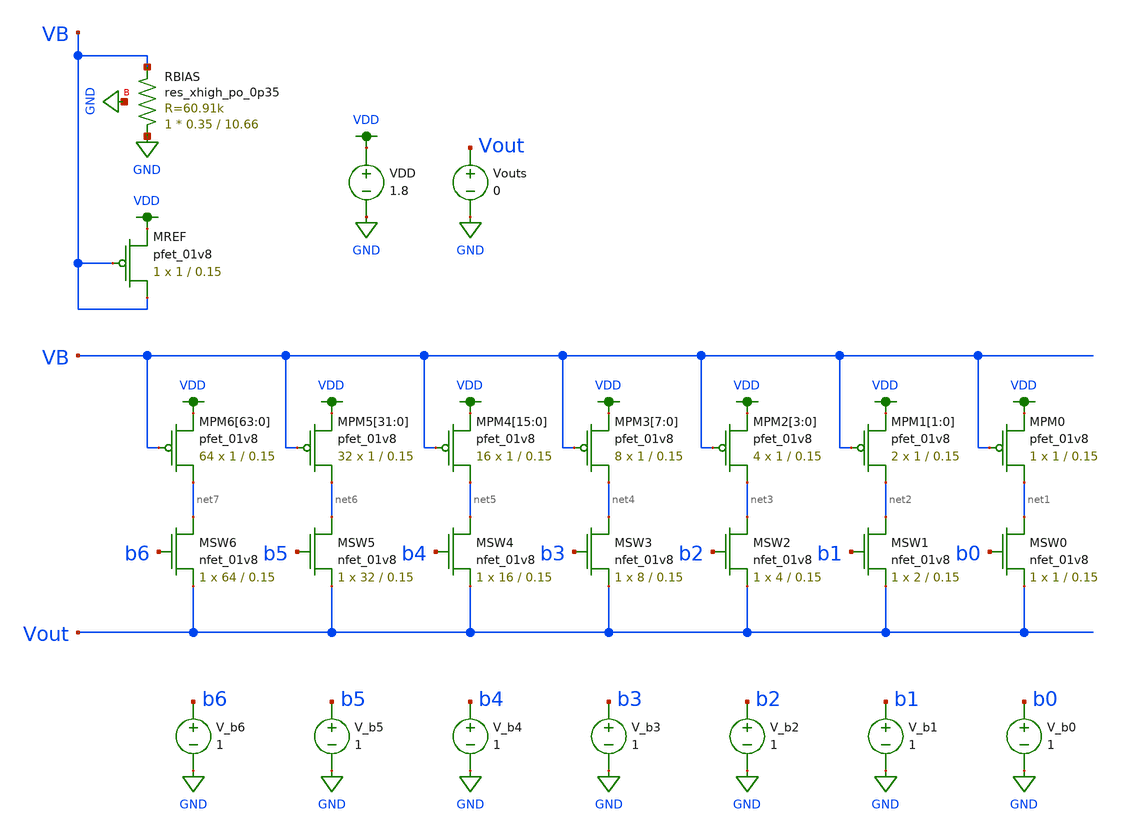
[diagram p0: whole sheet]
** sch_path: MP3/xschem/dac.sch
**.subckt dac
VDD VDD GND 1.8
XMREF VB VB VDD VDD sky130_fd_pr__pfet_01v8 L=0.15 W=1 nf=1 ad='int((nf+1)/2) * W/nf * 0.29' as='int((nf+2)/2) * W/nf * 0.29'
+ pd='2*int((nf+1)/2) * (W/nf + 0.29)' ps='2*int((nf+2)/2) * (W/nf + 0.29)' nrd='0.29 / W' nrs='0.29 / W'
+ sa=0 sb=0 sd=0 mult=1 m=1
XMPM6[63] net7 VB VDD VDD sky130_fd_pr__pfet_01v8 L=0.15 W=1 nf=1 ad='int((nf+1)/2) * W/nf * 0.29' as='int((nf+2)/2) * W/nf * 0.29'
+ pd='2*int((nf+1)/2) * (W/nf + 0.29)' ps='2*int((nf+2)/2) * (W/nf + 0.29)' nrd='0.29 / W' nrs='0.29 / W'
+ sa=0 sb=0 sd=0 mult=64 m=64
XMPM6[62] net7 VB VDD VDD sky130_fd_pr__pfet_01v8 L=0.15 W=1 nf=1 ad='int((nf+1)/2) * W/nf * 0.29' as='int((nf+2)/2) * W/nf * 0.29'
+ pd='2*int((nf+1)/2) * (W/nf + 0.29)' ps='2*int((nf+2)/2) * (W/nf + 0.29)' nrd='0.29 / W' nrs='0.29 / W'
+ sa=0 sb=0 sd=0 mult=64 m=64
XMPM6[61] net7 VB VDD VDD sky130_fd_pr__pfet_01v8 L=0.15 W=1 nf=1 ad='int((nf+1)/2) * W/nf * 0.29' as='int((nf+2)/2) * W/nf * 0.29'
+ pd='2*int((nf+1)/2) * (W/nf + 0.29)' ps='2*int((nf+2)/2) * (W/nf + 0.29)' nrd='0.29 / W' nrs='0.29 / W'
+ sa=0 sb=0 sd=0 mult=64 m=64
XMPM6[60] net7 VB VDD VDD sky130_fd_pr__pfet_01v8 L=0.15 W=1 nf=1 ad='int((nf+1)/2) * W/nf * 0.29' as='int((nf+2)/2) * W/nf * 0.29'
+ pd='2*int((nf+1)/2) * (W/nf + 0.29)' ps='2*int((nf+2)/2) * (W/nf + 0.29)' nrd='0.29 / W' nrs='0.29 / W'
+ sa=0 sb=0 sd=0 mult=64 m=64
XMPM6[59] net7 VB VDD VDD sky130_fd_pr__pfet_01v8 L=0.15 W=1 nf=1 ad='int((nf+1)/2) * W/nf * 0.29' as='int((nf+2)/2) * W/nf * 0.29'
+ pd='2*int((nf+1)/2) * (W/nf + 0.29)' ps='2*int((nf+2)/2) * (W/nf + 0.29)' nrd='0.29 / W' nrs='0.29 / W'
+ sa=0 sb=0 sd=0 mult=64 m=64
XMPM6[58] net7 VB VDD VDD sky130_fd_pr__pfet_01v8 L=0.15 W=1 nf=1 ad='int((nf+1)/2) * W/nf * 0.29' as='int((nf+2)/2) * W/nf * 0.29'
+ pd='2*int((nf+1)/2) * (W/nf + 0.29)' ps='2*int((nf+2)/2) * (W/nf + 0.29)' nrd='0.29 / W' nrs='0.29 / W'
+ sa=0 sb=0 sd=0 mult=64 m=64
XMPM6[57] net7 VB VDD VDD sky130_fd_pr__pfet_01v8 L=0.15 W=1 nf=1 ad='int((nf+1)/2) * W/nf * 0.29' as='int((nf+2)/2) * W/nf * 0.29'
+ pd='2*int((nf+1)/2) * (W/nf + 0.29)' ps='2*int((nf+2)/2) * (W/nf + 0.29)' nrd='0.29 / W' nrs='0.29 / W'
+ sa=0 sb=0 sd=0 mult=64 m=64
XMPM6[56] net7 VB VDD VDD sky130_fd_pr__pfet_01v8 L=0.15 W=1 nf=1 ad='int((nf+1)/2) * W/nf * 0.29' as='int((nf+2)/2) * W/nf * 0.29'
+ pd='2*int((nf+1)/2) * (W/nf + 0.29)' ps='2*int((nf+2)/2) * (W/nf + 0.29)' nrd='0.29 / W' nrs='0.29 / W'
+ sa=0 sb=0 sd=0 mult=64 m=64
XMPM6[55] net7 VB VDD VDD sky130_fd_pr__pfet_01v8 L=0.15 W=1 nf=1 ad='int((nf+1)/2) * W/nf * 0.29' as='int((nf+2)/2) * W/nf * 0.29'
+ pd='2*int((nf+1)/2) * (W/nf + 0.29)' ps='2*int((nf+2)/2) * (W/nf + 0.29)' nrd='0.29 / W' nrs='0.29 / W'
+ sa=0 sb=0 sd=0 mult=64 m=64
XMPM6[54] net7 VB VDD VDD sky130_fd_pr__pfet_01v8 L=0.15 W=1 nf=1 ad='int((nf+1)/2) * W/nf * 0.29' as='int((nf+2)/2) * W/nf * 0.29'
+ pd='2*int((nf+1)/2) * (W/nf + 0.29)' ps='2*int((nf+2)/2) * (W/nf + 0.29)' nrd='0.29 / W' nrs='0.29 / W'
+ sa=0 sb=0 sd=0 mult=64 m=64
XMPM6[53] net7 VB VDD VDD sky130_fd_pr__pfet_01v8 L=0.15 W=1 nf=1 ad='int((nf+1)/2) * W/nf * 0.29' as='int((nf+2)/2) * W/nf * 0.29'
+ pd='2*int((nf+1)/2) * (W/nf + 0.29)' ps='2*int((nf+2)/2) * (W/nf + 0.29)' nrd='0.29 / W' nrs='0.29 / W'
+ sa=0 sb=0 sd=0 mult=64 m=64
XMPM6[52] net7 VB VDD VDD sky130_fd_pr__pfet_01v8 L=0.15 W=1 nf=1 ad='int((nf+1)/2) * W/nf * 0.29' as='int((nf+2)/2) * W/nf * 0.29'
+ pd='2*int((nf+1)/2) * (W/nf + 0.29)' ps='2*int((nf+2)/2) * (W/nf + 0.29)' nrd='0.29 / W' nrs='0.29 / W'
+ sa=0 sb=0 sd=0 mult=64 m=64
XMPM6[51] net7 VB VDD VDD sky130_fd_pr__pfet_01v8 L=0.15 W=1 nf=1 ad='int((nf+1)/2) * W/nf * 0.29' as='int((nf+2)/2) * W/nf * 0.29'
+ pd='2*int((nf+1)/2) * (W/nf + 0.29)' ps='2*int((nf+2)/2) * (W/nf + 0.29)' nrd='0.29 / W' nrs='0.29 / W'
+ sa=0 sb=0 sd=0 mult=64 m=64
XMPM6[50] net7 VB VDD VDD sky130_fd_pr__pfet_01v8 L=0.15 W=1 nf=1 ad='int((nf+1)/2) * W/nf * 0.29' as='int((nf+2)/2) * W/nf * 0.29'
+ pd='2*int((nf+1)/2) * (W/nf + 0.29)' ps='2*int((nf+2)/2) * (W/nf + 0.29)' nrd='0.29 / W' nrs='0.29 / W'
+ sa=0 sb=0 sd=0 mult=64 m=64
XMPM6[49] net7 VB VDD VDD sky130_fd_pr__pfet_01v8 L=0.15 W=1 nf=1 ad='int((nf+1)/2) * W/nf * 0.29' as='int((nf+2)/2) * W/nf * 0.29'
+ pd='2*int((nf+1)/2) * (W/nf + 0.29)' ps='2*int((nf+2)/2) * (W/nf + 0.29)' nrd='0.29 / W' nrs='0.29 / W'
+ sa=0 sb=0 sd=0 mult=64 m=64
XMPM6[48] net7 VB VDD VDD sky130_fd_pr__pfet_01v8 L=0.15 W=1 nf=1 ad='int((nf+1)/2) * W/nf * 0.29' as='int((nf+2)/2) * W/nf * 0.29'
+ pd='2*int((nf+1)/2) * (W/nf + 0.29)' ps='2*int((nf+2)/2) * (W/nf + 0.29)' nrd='0.29 / W' nrs='0.29 / W'
+ sa=0 sb=0 sd=0 mult=64 m=64
XMPM6[47] net7 VB VDD VDD sky130_fd_pr__pfet_01v8 L=0.15 W=1 nf=1 ad='int((nf+1)/2) * W/nf * 0.29' as='int((nf+2)/2) * W/nf * 0.29'
+ pd='2*int((nf+1)/2) * (W/nf + 0.29)' ps='2*int((nf+2)/2) * (W/nf + 0.29)' nrd='0.29 / W' nrs='0.29 / W'
+ sa=0 sb=0 sd=0 mult=64 m=64
XMPM6[46] net7 VB VDD VDD sky130_fd_pr__pfet_01v8 L=0.15 W=1 nf=1 ad='int((nf+1)/2) * W/nf * 0.29' as='int((nf+2)/2) * W/nf * 0.29'
+ pd='2*int((nf+1)/2) * (W/nf + 0.29)' ps='2*int((nf+2)/2) * (W/nf + 0.29)' nrd='0.29 / W' nrs='0.29 / W'
+ sa=0 sb=0 sd=0 mult=64 m=64
XMPM6[45] net7 VB VDD VDD sky130_fd_pr__pfet_01v8 L=0.15 W=1 nf=1 ad='int((nf+1)/2) * W/nf * 0.29' as='int((nf+2)/2) * W/nf * 0.29'
+ pd='2*int((nf+1)/2) * (W/nf + 0.29)' ps='2*int((nf+2)/2) * (W/nf + 0.29)' nrd='0.29 / W' nrs='0.29 / W'
+ sa=0 sb=0 sd=0 mult=64 m=64
XMPM6[44] net7 VB VDD VDD sky130_fd_pr__pfet_01v8 L=0.15 W=1 nf=1 ad='int((nf+1)/2) * W/nf * 0.29' as='int((nf+2)/2) * W/nf * 0.29'
+ pd='2*int((nf+1)/2) * (W/nf + 0.29)' ps='2*int((nf+2)/2) * (W/nf + 0.29)' nrd='0.29 / W' nrs='0.29 / W'
+ sa=0 sb=0 sd=0 mult=64 m=64
XMPM6[43] net7 VB VDD VDD sky130_fd_pr__pfet_01v8 L=0.15 W=1 nf=1 ad='int((nf+1)/2) * W/nf * 0.29' as='int((nf+2)/2) * W/nf * 0.29'
+ pd='2*int((nf+1)/2) * (W/nf + 0.29)' ps='2*int((nf+2)/2) * (W/nf + 0.29)' nrd='0.29 / W' nrs='0.29 / W'
+ sa=0 sb=0 sd=0 mult=64 m=64
XMPM6[42] net7 VB VDD VDD sky130_fd_pr__pfet_01v8 L=0.15 W=1 nf=1 ad='int((nf+1)/2) * W/nf * 0.29' as='int((nf+2)/2) * W/nf * 0.29'
+ pd='2*int((nf+1)/2) * (W/nf + 0.29)' ps='2*int((nf+2)/2) * (W/nf + 0.29)' nrd='0.29 / W' nrs='0.29 / W'
+ sa=0 sb=0 sd=0 mult=64 m=64
XMPM6[41] net7 VB VDD VDD sky130_fd_pr__pfet_01v8 L=0.15 W=1 nf=1 ad='int((nf+1)/2) * W/nf * 0.29' as='int((nf+2)/2) * W/nf * 0.29'
+ pd='2*int((nf+1)/2) * (W/nf + 0.29)' ps='2*int((nf+2)/2) * (W/nf + 0.29)' nrd='0.29 / W' nrs='0.29 / W'
+ sa=0 sb=0 sd=0 mult=64 m=64
XMPM6[40] net7 VB VDD VDD sky130_fd_pr__pfet_01v8 L=0.15 W=1 nf=1 ad='int((nf+1)/2) * W/nf * 0.29' as='int((nf+2)/2) * W/nf * 0.29'
+ pd='2*int((nf+1)/2) * (W/nf + 0.29)' ps='2*int((nf+2)/2) * (W/nf + 0.29)' nrd='0.29 / W' nrs='0.29 / W'
+ sa=0 sb=0 sd=0 mult=64 m=64
XMPM6[39] net7 VB VDD VDD sky130_fd_pr__pfet_01v8 L=0.15 W=1 nf=1 ad='int((nf+1)/2) * W/nf * 0.29' as='int((nf+2)/2) * W/nf * 0.29'
+ pd='2*int((nf+1)/2) * (W/nf + 0.29)' ps='2*int((nf+2)/2) * (W/nf + 0.29)' nrd='0.29 / W' nrs='0.29 / W'
+ sa=0 sb=0 sd=0 mult=64 m=64
XMPM6[38] net7 VB VDD VDD sky130_fd_pr__pfet_01v8 L=0.15 W=1 nf=1 ad='int((nf+1)/2) * W/nf * 0.29' as='int((nf+2)/2) * W/nf * 0.29'
+ pd='2*int((nf+1)/2) * (W/nf + 0.29)' ps='2*int((nf+2)/2) * (W/nf + 0.29)' nrd='0.29 / W' nrs='0.29 / W'
+ sa=0 sb=0 sd=0 mult=64 m=64
XMPM6[37] net7 VB VDD VDD sky130_fd_pr__pfet_01v8 L=0.15 W=1 nf=1 ad='int((nf+1)/2) * W/nf * 0.29' as='int((nf+2)/2) * W/nf * 0.29'
+ pd='2*int((nf+1)/2) * (W/nf + 0.29)' ps='2*int((nf+2)/2) * (W/nf + 0.29)' nrd='0.29 / W' nrs='0.29 / W'
+ sa=0 sb=0 sd=0 mult=64 m=64
XMPM6[36] net7 VB VDD VDD sky130_fd_pr__pfet_01v8 L=0.15 W=1 nf=1 ad='int((nf+1)/2) * W/nf * 0.29' as='int((nf+2)/2) * W/nf * 0.29'
+ pd='2*int((nf+1)/2) * (W/nf + 0.29)' ps='2*int((nf+2)/2) * (W/nf + 0.29)' nrd='0.29 / W' nrs='0.29 / W'
+ sa=0 sb=0 sd=0 mult=64 m=64
XMPM6[35] net7 VB VDD VDD sky130_fd_pr__pfet_01v8 L=0.15 W=1 nf=1 ad='int((nf+1)/2) * W/nf * 0.29' as='int((nf+2)/2) * W/nf * 0.29'
+ pd='2*int((nf+1)/2) * (W/nf + 0.29)' ps='2*int((nf+2)/2) * (W/nf + 0.29)' nrd='0.29 / W' nrs='0.29 / W'
+ sa=0 sb=0 sd=0 mult=64 m=64
XMPM6[34] net7 VB VDD VDD sky130_fd_pr__pfet_01v8 L=0.15 W=1 nf=1 ad='int((nf+1)/2) * W/nf * 0.29' as='int((nf+2)/2) * W/nf * 0.29'
+ pd='2*int((nf+1)/2) * (W/nf + 0.29)' ps='2*int((nf+2)/2) * (W/nf + 0.29)' nrd='0.29 / W' nrs='0.29 / W'
+ sa=0 sb=0 sd=0 mult=64 m=64
XMPM6[33] net7 VB VDD VDD sky130_fd_pr__pfet_01v8 L=0.15 W=1 nf=1 ad='int((nf+1)/2) * W/nf * 0.29' as='int((nf+2)/2) * W/nf * 0.29'
+ pd='2*int((nf+1)/2) * (W/nf + 0.29)' ps='2*int((nf+2)/2) * (W/nf + 0.29)' nrd='0.29 / W' nrs='0.29 / W'
+ sa=0 sb=0 sd=0 mult=64 m=64
XMPM6[32] net7 VB VDD VDD sky130_fd_pr__pfet_01v8 L=0.15 W=1 nf=1 ad='int((nf+1)/2) * W/nf * 0.29' as='int((nf+2)/2) * W/nf * 0.29'
+ pd='2*int((nf+1)/2) * (W/nf + 0.29)' ps='2*int((nf+2)/2) * (W/nf + 0.29)' nrd='0.29 / W' nrs='0.29 / W'
+ sa=0 sb=0 sd=0 mult=64 m=64
XMPM6[31] net7 VB VDD VDD sky130_fd_pr__pfet_01v8 L=0.15 W=1 nf=1 ad='int((nf+1)/2) * W/nf * 0.29' as='int((nf+2)/2) * W/nf * 0.29'
+ pd='2*int((nf+1)/2) * (W/nf + 0.29)' ps='2*int((nf+2)/2) * (W/nf + 0.29)' nrd='0.29 / W' nrs='0.29 / W'
+ sa=0 sb=0 sd=0 mult=64 m=64
XMPM6[30] net7 VB VDD VDD sky130_fd_pr__pfet_01v8 L=0.15 W=1 nf=1 ad='int((nf+1)/2) * W/nf * 0.29' as='int((nf+2)/2) * W/nf * 0.29'
+ pd='2*int((nf+1)/2) * (W/nf + 0.29)' ps='2*int((nf+2)/2) * (W/nf + 0.29)' nrd='0.29 / W' nrs='0.29 / W'
+ sa=0 sb=0 sd=0 mult=64 m=64
XMPM6[29] net7 VB VDD VDD sky130_fd_pr__pfet_01v8 L=0.15 W=1 nf=1 ad='int((nf+1)/2) * W/nf * 0.29' as='int((nf+2)/2) * W/nf * 0.29'
+ pd='2*int((nf+1)/2) * (W/nf + 0.29)' ps='2*int((nf+2)/2) * (W/nf + 0.29)' nrd='0.29 / W' nrs='0.29 / W'
+ sa=0 sb=0 sd=0 mult=64 m=64
XMPM6[28] net7 VB VDD VDD sky130_fd_pr__pfet_01v8 L=0.15 W=1 nf=1 ad='int((nf+1)/2) * W/nf * 0.29' as='int((nf+2)/2) * W/nf * 0.29'
+ pd='2*int((nf+1)/2) * (W/nf + 0.29)' ps='2*int((nf+2)/2) * (W/nf + 0.29)' nrd='0.29 / W' nrs='0.29 / W'
+ sa=0 sb=0 sd=0 mult=64 m=64
XMPM6[27] net7 VB VDD VDD sky130_fd_pr__pfet_01v8 L=0.15 W=1 nf=1 ad='int((nf+1)/2) * W/nf * 0.29' as='int((nf+2)/2) * W/nf * 0.29'
+ pd='2*int((nf+1)/2) * (W/nf + 0.29)' ps='2*int((nf+2)/2) * (W/nf + 0.29)' nrd='0.29 / W' nrs='0.29 / W'
+ sa=0 sb=0 sd=0 mult=64 m=64
XMPM6[26] net7 VB VDD VDD sky130_fd_pr__pfet_01v8 L=0.15 W=1 nf=1 ad='int((nf+1)/2) * W/nf * 0.29' as='int((nf+2)/2) * W/nf * 0.29'
+ pd='2*int((nf+1)/2) * (W/nf + 0.29)' ps='2*int((nf+2)/2) * (W/nf + 0.29)' nrd='0.29 / W' nrs='0.29 / W'
+ sa=0 sb=0 sd=0 mult=64 m=64
XMPM6[25] net7 VB VDD VDD sky130_fd_pr__pfet_01v8 L=0.15 W=1 nf=1 ad='int((nf+1)/2) * W/nf * 0.29' as='int((nf+2)/2) * W/nf * 0.29'
+ pd='2*int((nf+1)/2) * (W/nf + 0.29)' ps='2*int((nf+2)/2) * (W/nf + 0.29)' nrd='0.29 / W' nrs='0.29 / W'
+ sa=0 sb=0 sd=0 mult=64 m=64
XMPM6[24] net7 VB VDD VDD sky130_fd_pr__pfet_01v8 L=0.15 W=1 nf=1 ad='int((nf+1)/2) * W/nf * 0.29' as='int((nf+2)/2) * W/nf * 0.29'
+ pd='2*int((nf+1)/2) * (W/nf + 0.29)' ps='2*int((nf+2)/2) * (W/nf + 0.29)' nrd='0.29 / W' nrs='0.29 / W'
+ sa=0 sb=0 sd=0 mult=64 m=64
XMPM6[23] net7 VB VDD VDD sky130_fd_pr__pfet_01v8 L=0.15 W=1 nf=1 ad='int((nf+1)/2) * W/nf * 0.29' as='int((nf+2)/2) * W/nf * 0.29'
+ pd='2*int((nf+1)/2) * (W/nf + 0.29)' ps='2*int((nf+2)/2) * (W/nf + 0.29)' nrd='0.29 / W' nrs='0.29 / W'
+ sa=0 sb=0 sd=0 mult=64 m=64
XMPM6[22] net7 VB VDD VDD sky130_fd_pr__pfet_01v8 L=0.15 W=1 nf=1 ad='int((nf+1)/2) * W/nf * 0.29' as='int((nf+2)/2) * W/nf * 0.29'
+ pd='2*int((nf+1)/2) * (W/nf + 0.29)' ps='2*int((nf+2)/2) * (W/nf + 0.29)' nrd='0.29 / W' nrs='0.29 / W'
+ sa=0 sb=0 sd=0 mult=64 m=64
XMPM6[21] net7 VB VDD VDD sky130_fd_pr__pfet_01v8 L=0.15 W=1 nf=1 ad='int((nf+1)/2) * W/nf * 0.29' as='int((nf+2)/2) * W/nf * 0.29'
+ pd='2*int((nf+1)/2) * (W/nf + 0.29)' ps='2*int((nf+2)/2) * (W/nf + 0.29)' nrd='0.29 / W' nrs='0.29 / W'
+ sa=0 sb=0 sd=0 mult=64 m=64
XMPM6[20] net7 VB VDD VDD sky130_fd_pr__pfet_01v8 L=0.15 W=1 nf=1 ad='int((nf+1)/2) * W/nf * 0.29' as='int((nf+2)/2) * W/nf * 0.29'
+ pd='2*int((nf+1)/2) * (W/nf + 0.29)' ps='2*int((nf+2)/2) * (W/nf + 0.29)' nrd='0.29 / W' nrs='0.29 / W'
+ sa=0 sb=0 sd=0 mult=64 m=64
XMPM6[19] net7 VB VDD VDD sky130_fd_pr__pfet_01v8 L=0.15 W=1 nf=1 ad='int((nf+1)/2) * W/nf * 0.29' as='int((nf+2)/2) * W/nf * 0.29'
+ pd='2*int((nf+1)/2) * (W/nf + 0.29)' ps='2*int((nf+2)/2) * (W/nf + 0.29)' nrd='0.29 / W' nrs='0.29 / W'
+ sa=0 sb=0 sd=0 mult=64 m=64
XMPM6[18] net7 VB VDD VDD sky130_fd_pr__pfet_01v8 L=0.15 W=1 nf=1 ad='int((nf+1)/2) * W/nf * 0.29' as='int((nf+2)/2) * W/nf * 0.29'
+ pd='2*int((nf+1)/2) * (W/nf + 0.29)' ps='2*int((nf+2)/2) * (W/nf + 0.29)' nrd='0.29 / W' nrs='0.29 / W'
+ sa=0 sb=0 sd=0 mult=64 m=64
XMPM6[17] net7 VB VDD VDD sky130_fd_pr__pfet_01v8 L=0.15 W=1 nf=1 ad='int((nf+1)/2) * W/nf * 0.29' as='int((nf+2)/2) * W/nf * 0.29'
+ pd='2*int((nf+1)/2) * (W/nf + 0.29)' ps='2*int((nf+2)/2) * (W/nf + 0.29)' nrd='0.29 / W' nrs='0.29 / W'
+ sa=0 sb=0 sd=0 mult=64 m=64
XMPM6[16] net7 VB VDD VDD sky130_fd_pr__pfet_01v8 L=0.15 W=1 nf=1 ad='int((nf+1)/2) * W/nf * 0.29' as='int((nf+2)/2) * W/nf * 0.29'
+ pd='2*int((nf+1)/2) * (W/nf + 0.29)' ps='2*int((nf+2)/2) * (W/nf + 0.29)' nrd='0.29 / W' nrs='0.29 / W'
+ sa=0 sb=0 sd=0 mult=64 m=64
XMPM6[15] net7 VB VDD VDD sky130_fd_pr__pfet_01v8 L=0.15 W=1 nf=1 ad='int((nf+1)/2) * W/nf * 0.29' as='int((nf+2)/2) * W/nf * 0.29'
+ pd='2*int((nf+1)/2) * (W/nf + 0.29)' ps='2*int((nf+2)/2) * (W/nf + 0.29)' nrd='0.29 / W' nrs='0.29 / W'
+ sa=0 sb=0 sd=0 mult=64 m=64
XMPM6[14] net7 VB VDD VDD sky130_fd_pr__pfet_01v8 L=0.15 W=1 nf=1 ad='int((nf+1)/2) * W/nf * 0.29' as='int((nf+2)/2) * W/nf * 0.29'
+ pd='2*int((nf+1)/2) * (W/nf + 0.29)' ps='2*int((nf+2)/2) * (W/nf + 0.29)' nrd='0.29 / W' nrs='0.29 / W'
+ sa=0 sb=0 sd=0 mult=64 m=64
XMPM6[13] net7 VB VDD VDD sky130_fd_pr__pfet_01v8 L=0.15 W=1 nf=1 ad='int((nf+1)/2) * W/nf * 0.29' as='int((nf+2)/2) * W/nf * 0.29'
+ pd='2*int((nf+1)/2) * (W/nf + 0.29)' ps='2*int((nf+2)/2) * (W/nf + 0.29)' nrd='0.29 / W' nrs='0.29 / W'
+ sa=0 sb=0 sd=0 mult=64 m=64
XMPM6[12] net7 VB VDD VDD sky130_fd_pr__pfet_01v8 L=0.15 W=1 nf=1 ad='int((nf+1)/2) * W/nf * 0.29' as='int((nf+2)/2) * W/nf * 0.29'
+ pd='2*int((nf+1)/2) * (W/nf + 0.29)' ps='2*int((nf+2)/2) * (W/nf + 0.29)' nrd='0.29 / W' nrs='0.29 / W'
+ sa=0 sb=0 sd=0 mult=64 m=64
XMPM6[11] net7 VB VDD VDD sky130_fd_pr__pfet_01v8 L=0.15 W=1 nf=1 ad='int((nf+1)/2) * W/nf * 0.29' as='int((nf+2)/2) * W/nf * 0.29'
+ pd='2*int((nf+1)/2) * (W/nf + 0.29)' ps='2*int((nf+2)/2) * (W/nf + 0.29)' nrd='0.29 / W' nrs='0.29 / W'
+ sa=0 sb=0 sd=0 mult=64 m=64
XMPM6[10] net7 VB VDD VDD sky130_fd_pr__pfet_01v8 L=0.15 W=1 nf=1 ad='int((nf+1)/2) * W/nf * 0.29' as='int((nf+2)/2) * W/nf * 0.29'
+ pd='2*int((nf+1)/2) * (W/nf + 0.29)' ps='2*int((nf+2)/2) * (W/nf + 0.29)' nrd='0.29 / W' nrs='0.29 / W'
+ sa=0 sb=0 sd=0 mult=64 m=64
XMPM6[9] net7 VB VDD VDD sky130_fd_pr__pfet_01v8 L=0.15 W=1 nf=1 ad='int((nf+1)/2) * W/nf * 0.29' as='int((nf+2)/2) * W/nf * 0.29'
+ pd='2*int((nf+1)/2) * (W/nf + 0.29)' ps='2*int((nf+2)/2) * (W/nf + 0.29)' nrd='0.29 / W' nrs='0.29 / W'
+ sa=0 sb=0 sd=0 mult=64 m=64
XMPM6[8] net7 VB VDD VDD sky130_fd_pr__pfet_01v8 L=0.15 W=1 nf=1 ad='int((nf+1)/2) * W/nf * 0.29' as='int((nf+2)/2) * W/nf * 0.29'
+ pd='2*int((nf+1)/2) * (W/nf + 0.29)' ps='2*int((nf+2)/2) * (W/nf + 0.29)' nrd='0.29 / W' nrs='0.29 / W'
+ sa=0 sb=0 sd=0 mult=64 m=64
XMPM6[7] net7 VB VDD VDD sky130_fd_pr__pfet_01v8 L=0.15 W=1 nf=1 ad='int((nf+1)/2) * W/nf * 0.29' as='int((nf+2)/2) * W/nf * 0.29'
+ pd='2*int((nf+1)/2) * (W/nf + 0.29)' ps='2*int((nf+2)/2) * (W/nf + 0.29)' nrd='0.29 / W' nrs='0.29 / W'
+ sa=0 sb=0 sd=0 mult=64 m=64
XMPM6[6] net7 VB VDD VDD sky130_fd_pr__pfet_01v8 L=0.15 W=1 nf=1 ad='int((nf+1)/2) * W/nf * 0.29' as='int((nf+2)/2) * W/nf * 0.29'
+ pd='2*int((nf+1)/2) * (W/nf + 0.29)' ps='2*int((nf+2)/2) * (W/nf + 0.29)' nrd='0.29 / W' nrs='0.29 / W'
+ sa=0 sb=0 sd=0 mult=64 m=64
XMPM6[5] net7 VB VDD VDD sky130_fd_pr__pfet_01v8 L=0.15 W=1 nf=1 ad='int((nf+1)/2) * W/nf * 0.29' as='int((nf+2)/2) * W/nf * 0.29'
+ pd='2*int((nf+1)/2) * (W/nf + 0.29)' ps='2*int((nf+2)/2) * (W/nf + 0.29)' nrd='0.29 / W' nrs='0.29 / W'
+ sa=0 sb=0 sd=0 mult=64 m=64
XMPM6[4] net7 VB VDD VDD sky130_fd_pr__pfet_01v8 L=0.15 W=1 nf=1 ad='int((nf+1)/2) * W/nf * 0.29' as='int((nf+2)/2) * W/nf * 0.29'
+ pd='2*int((nf+1)/2) * (W/nf + 0.29)' ps='2*int((nf+2)/2) * (W/nf + 0.29)' nrd='0.29 / W' nrs='0.29 / W'
+ sa=0 sb=0 sd=0 mult=64 m=64
XMPM6[3] net7 VB VDD VDD sky130_fd_pr__pfet_01v8 L=0.15 W=1 nf=1 ad='int((nf+1)/2) * W/nf * 0.29' as='int((nf+2)/2) * W/nf * 0.29'
+ pd='2*int((nf+1)/2) * (W/nf + 0.29)' ps='2*int((nf+2)/2) * (W/nf + 0.29)' nrd='0.29 / W' nrs='0.29 / W'
+ sa=0 sb=0 sd=0 mult=64 m=64
XMPM6[2] net7 VB VDD VDD sky130_fd_pr__pfet_01v8 L=0.15 W=1 nf=1 ad='int((nf+1)/2) * W/nf * 0.29' as='int((nf+2)/2) * W/nf * 0.29'
+ pd='2*int((nf+1)/2) * (W/nf + 0.29)' ps='2*int((nf+2)/2) * (W/nf + 0.29)' nrd='0.29 / W' nrs='0.29 / W'
+ sa=0 sb=0 sd=0 mult=64 m=64
XMPM6[1] net7 VB VDD VDD sky130_fd_pr__pfet_01v8 L=0.15 W=1 nf=1 ad='int((nf+1)/2) * W/nf * 0.29' as='int((nf+2)/2) * W/nf * 0.29'
+ pd='2*int((nf+1)/2) * (W/nf + 0.29)' ps='2*int((nf+2)/2) * (W/nf + 0.29)' nrd='0.29 / W' nrs='0.29 / W'
+ sa=0 sb=0 sd=0 mult=64 m=64
XMPM6[0] net7 VB VDD VDD sky130_fd_pr__pfet_01v8 L=0.15 W=1 nf=1 ad='int((nf+1)/2) * W/nf * 0.29' as='int((nf+2)/2) * W/nf * 0.29'
+ pd='2*int((nf+1)/2) * (W/nf + 0.29)' ps='2*int((nf+2)/2) * (W/nf + 0.29)' nrd='0.29 / W' nrs='0.29 / W'
+ sa=0 sb=0 sd=0 mult=64 m=64
XMPM5[31] net6 VB VDD VDD sky130_fd_pr__pfet_01v8 L=0.15 W=1 nf=1 ad='int((nf+1)/2) * W/nf * 0.29' as='int((nf+2)/2) * W/nf * 0.29'
+ pd='2*int((nf+1)/2) * (W/nf + 0.29)' ps='2*int((nf+2)/2) * (W/nf + 0.29)' nrd='0.29 / W' nrs='0.29 / W'
+ sa=0 sb=0 sd=0 mult=32 m=32
XMPM5[30] net6 VB VDD VDD sky130_fd_pr__pfet_01v8 L=0.15 W=1 nf=1 ad='int((nf+1)/2) * W/nf * 0.29' as='int((nf+2)/2) * W/nf * 0.29'
+ pd='2*int((nf+1)/2) * (W/nf + 0.29)' ps='2*int((nf+2)/2) * (W/nf + 0.29)' nrd='0.29 / W' nrs='0.29 / W'
+ sa=0 sb=0 sd=0 mult=32 m=32
XMPM5[29] net6 VB VDD VDD sky130_fd_pr__pfet_01v8 L=0.15 W=1 nf=1 ad='int((nf+1)/2) * W/nf * 0.29' as='int((nf+2)/2) * W/nf * 0.29'
+ pd='2*int((nf+1)/2) * (W/nf + 0.29)' ps='2*int((nf+2)/2) * (W/nf + 0.29)' nrd='0.29 / W' nrs='0.29 / W'
+ sa=0 sb=0 sd=0 mult=32 m=32
XMPM5[28] net6 VB VDD VDD sky130_fd_pr__pfet_01v8 L=0.15 W=1 nf=1 ad='int((nf+1)/2) * W/nf * 0.29' as='int((nf+2)/2) * W/nf * 0.29'
+ pd='2*int((nf+1)/2) * (W/nf + 0.29)' ps='2*int((nf+2)/2) * (W/nf + 0.29)' nrd='0.29 / W' nrs='0.29 / W'
+ sa=0 sb=0 sd=0 mult=32 m=32
XMPM5[27] net6 VB VDD VDD sky130_fd_pr__pfet_01v8 L=0.15 W=1 nf=1 ad='int((nf+1)/2) * W/nf * 0.29' as='int((nf+2)/2) * W/nf * 0.29'
+ pd='2*int((nf+1)/2) * (W/nf + 0.29)' ps='2*int((nf+2)/2) * (W/nf + 0.29)' nrd='0.29 / W' nrs='0.29 / W'
+ sa=0 sb=0 sd=0 mult=32 m=32
XMPM5[26] net6 VB VDD VDD sky130_fd_pr__pfet_01v8 L=0.15 W=1 nf=1 ad='int((nf+1)/2) * W/nf * 0.29' as='int((nf+2)/2) * W/nf * 0.29'
+ pd='2*int((nf+1)/2) * (W/nf + 0.29)' ps='2*int((nf+2)/2) * (W/nf + 0.29)' nrd='0.29 / W' nrs='0.29 / W'
+ sa=0 sb=0 sd=0 mult=32 m=32
XMPM5[25] net6 VB VDD VDD sky130_fd_pr__pfet_01v8 L=0.15 W=1 nf=1 ad='int((nf+1)/2) * W/nf * 0.29' as='int((nf+2)/2) * W/nf * 0.29'
+ pd='2*int((nf+1)/2) * (W/nf + 0.29)' ps='2*int((nf+2)/2) * (W/nf + 0.29)' nrd='0.29 / W' nrs='0.29 / W'
+ sa=0 sb=0 sd=0 mult=32 m=32
XMPM5[24] net6 VB VDD VDD sky130_fd_pr__pfet_01v8 L=0.15 W=1 nf=1 ad='int((nf+1)/2) * W/nf * 0.29' as='int((nf+2)/2) * W/nf * 0.29'
+ pd='2*int((nf+1)/2) * (W/nf + 0.29)' ps='2*int((nf+2)/2) * (W/nf + 0.29)' nrd='0.29 / W' nrs='0.29 / W'
+ sa=0 sb=0 sd=0 mult=32 m=32
XMPM5[23] net6 VB VDD VDD sky130_fd_pr__pfet_01v8 L=0.15 W=1 nf=1 ad='int((nf+1)/2) * W/nf * 0.29' as='int((nf+2)/2) * W/nf * 0.29'
+ pd='2*int((nf+1)/2) * (W/nf + 0.29)' ps='2*int((nf+2)/2) * (W/nf + 0.29)' nrd='0.29 / W' nrs='0.29 / W'
+ sa=0 sb=0 sd=0 mult=32 m=32
XMPM5[22] net6 VB VDD VDD sky130_fd_pr__pfet_01v8 L=0.15 W=1 nf=1 ad='int((nf+1)/2) * W/nf * 0.29' as='int((nf+2)/2) * W/nf * 0.29'
+ pd='2*int((nf+1)/2) * (W/nf + 0.29)' ps='2*int((nf+2)/2) * (W/nf + 0.29)' nrd='0.29 / W' nrs='0.29 / W'
+ sa=0 sb=0 sd=0 mult=32 m=32
XMPM5[21] net6 VB VDD VDD sky130_fd_pr__pfet_01v8 L=0.15 W=1 nf=1 ad='int((nf+1)/2) * W/nf * 0.29' as='int((nf+2)/2) * W/nf * 0.29'
+ pd='2*int((nf+1)/2) * (W/nf + 0.29)' ps='2*int((nf+2)/2) * (W/nf + 0.29)' nrd='0.29 / W' nrs='0.29 / W'
+ sa=0 sb=0 sd=0 mult=32 m=32
XMPM5[20] net6 VB VDD VDD sky130_fd_pr__pfet_01v8 L=0.15 W=1 nf=1 ad='int((nf+1)/2) * W/nf * 0.29' as='int((nf+2)/2) * W/nf * 0.29'
+ pd='2*int((nf+1)/2) * (W/nf + 0.29)' ps='2*int((nf+2)/2) * (W/nf + 0.29)' nrd='0.29 / W' nrs='0.29 / W'
+ sa=0 sb=0 sd=0 mult=32 m=32
XMPM5[19] net6 VB VDD VDD sky130_fd_pr__pfet_01v8 L=0.15 W=1 nf=1 ad='int((nf+1)/2) * W/nf * 0.29' as='int((nf+2)/2) * W/nf * 0.29'
+ pd='2*int((nf+1)/2) * (W/nf + 0.29)' ps='2*int((nf+2)/2) * (W/nf + 0.29)' nrd='0.29 / W' nrs='0.29 / W'
+ sa=0 sb=0 sd=0 mult=32 m=32
XMPM5[18] net6 VB VDD VDD sky130_fd_pr__pfet_01v8 L=0.15 W=1 nf=1 ad='int((nf+1)/2) * W/nf * 0.29' as='int((nf+2)/2) * W/nf * 0.29'
+ pd='2*int((nf+1)/2) * (W/nf + 0.29)' ps='2*int((nf+2)/2) * (W/nf + 0.29)' nrd='0.29 / W' nrs='0.29 / W'
+ sa=0 sb=0 sd=0 mult=32 m=32
XMPM5[17] net6 VB VDD VDD sky130_fd_pr__pfet_01v8 L=0.15 W=1 nf=1 ad='int((nf+1)/2) * W/nf * 0.29' as='int((nf+2)/2) * W/nf * 0.29'
+ pd='2*int((nf+1)/2) * (W/nf + 0.29)' ps='2*int((nf+2)/2) * (W/nf + 0.29)' nrd='0.29 / W' nrs='0.29 / W'
+ sa=0 sb=0 sd=0 mult=32 m=32
XMPM5[16] net6 VB VDD VDD sky130_fd_pr__pfet_01v8 L=0.15 W=1 nf=1 ad='int((nf+1)/2) * W/nf * 0.29' as='int((nf+2)/2) * W/nf * 0.29'
+ pd='2*int((nf+1)/2) * (W/nf + 0.29)' ps='2*int((nf+2)/2) * (W/nf + 0.29)' nrd='0.29 / W' nrs='0.29 / W'
+ sa=0 sb=0 sd=0 mult=32 m=32
XMPM5[15] net6 VB VDD VDD sky130_fd_pr__pfet_01v8 L=0.15 W=1 nf=1 ad='int((nf+1)/2) * W/nf * 0.29' as='int((nf+2)/2) * W/nf * 0.29'
+ pd='2*int((nf+1)/2) * (W/nf + 0.29)' ps='2*int((nf+2)/2) * (W/nf + 0.29)' nrd='0.29 / W' nrs='0.29 / W'
+ sa=0 sb=0 sd=0 mult=32 m=32
XMPM5[14] net6 VB VDD VDD sky130_fd_pr__pfet_01v8 L=0.15 W=1 nf=1 ad='int((nf+1)/2) * W/nf * 0.29' as='int((nf+2)/2) * W/nf * 0.29'
+ pd='2*int((nf+1)/2) * (W/nf + 0.29)' ps='2*int((nf+2)/2) * (W/nf + 0.29)' nrd='0.29 / W' nrs='0.29 / W'
+ sa=0 sb=0 sd=0 mult=32 m=32
XMPM5[13] net6 VB VDD VDD sky130_fd_pr__pfet_01v8 L=0.15 W=1 nf=1 ad='int((nf+1)/2) * W/nf * 0.29' as='int((nf+2)/2) * W/nf * 0.29'
+ pd='2*int((nf+1)/2) * (W/nf + 0.29)' ps='2*int((nf+2)/2) * (W/nf + 0.29)' nrd='0.29 / W' nrs='0.29 / W'
+ sa=0 sb=0 sd=0 mult=32 m=32
XMPM5[12] net6 VB VDD VDD sky130_fd_pr__pfet_01v8 L=0.15 W=1 nf=1 ad='int((nf+1)/2) * W/nf * 0.29' as='int((nf+2)/2) * W/nf * 0.29'
+ pd='2*int((nf+1)/2) * (W/nf + 0.29)' ps='2*int((nf+2)/2) * (W/nf + 0.29)' nrd='0.29 / W' nrs='0.29 / W'
+ sa=0 sb=0 sd=0 mult=32 m=32
XMPM5[11] net6 VB VDD VDD sky130_fd_pr__pfet_01v8 L=0.15 W=1 nf=1 ad='int((nf+1)/2) * W/nf * 0.29' as='int((nf+2)/2) * W/nf * 0.29'
+ pd='2*int((nf+1)/2) * (W/nf + 0.29)' ps='2*int((nf+2)/2) * (W/nf + 0.29)' nrd='0.29 / W' nrs='0.29 / W'
+ sa=0 sb=0 sd=0 mult=32 m=32
XMPM5[10] net6 VB VDD VDD sky130_fd_pr__pfet_01v8 L=0.15 W=1 nf=1 ad='int((nf+1)/2) * W/nf * 0.29' as='int((nf+2)/2) * W/nf * 0.29'
+ pd='2*int((nf+1)/2) * (W/nf + 0.29)' ps='2*int((nf+2)/2) * (W/nf + 0.29)' nrd='0.29 / W' nrs='0.29 / W'
+ sa=0 sb=0 sd=0 mult=32 m=32
XMPM5[9] net6 VB VDD VDD sky130_fd_pr__pfet_01v8 L=0.15 W=1 nf=1 ad='int((nf+1)/2) * W/nf * 0.29' as='int((nf+2)/2) * W/nf * 0.29'
+ pd='2*int((nf+1)/2) * (W/nf + 0.29)' ps='2*int((nf+2)/2) * (W/nf + 0.29)' nrd='0.29 / W' nrs='0.29 / W'
+ sa=0 sb=0 sd=0 mult=32 m=32
XMPM5[8] net6 VB VDD VDD sky130_fd_pr__pfet_01v8 L=0.15 W=1 nf=1 ad='int((nf+1)/2) * W/nf * 0.29' as='int((nf+2)/2) * W/nf * 0.29'
+ pd='2*int((nf+1)/2) * (W/nf + 0.29)' ps='2*int((nf+2)/2) * (W/nf + 0.29)' nrd='0.29 / W' nrs='0.29 / W'
+ sa=0 sb=0 sd=0 mult=32 m=32
XMPM5[7] net6 VB VDD VDD sky130_fd_pr__pfet_01v8 L=0.15 W=1 nf=1 ad='int((nf+1)/2) * W/nf * 0.29' as='int((nf+2)/2) * W/nf * 0.29'
+ pd='2*int((nf+1)/2) * (W/nf + 0.29)' ps='2*int((nf+2)/2) * (W/nf + 0.29)' nrd='0.29 / W' nrs='0.29 / W'
+ sa=0 sb=0 sd=0 mult=32 m=32
XMPM5[6] net6 VB VDD VDD sky130_fd_pr__pfet_01v8 L=0.15 W=1 nf=1 ad='int((nf+1)/2) * W/nf * 0.29' as='int((nf+2)/2) * W/nf * 0.29'
+ pd='2*int((nf+1)/2) * (W/nf + 0.29)' ps='2*int((nf+2)/2) * (W/nf + 0.29)' nrd='0.29 / W' nrs='0.29 / W'
+ sa=0 sb=0 sd=0 mult=32 m=32
XMPM5[5] net6 VB VDD VDD sky130_fd_pr__pfet_01v8 L=0.15 W=1 nf=1 ad='int((nf+1)/2) * W/nf * 0.29' as='int((nf+2)/2) * W/nf * 0.29'
+ pd='2*int((nf+1)/2) * (W/nf + 0.29)' ps='2*int((nf+2)/2) * (W/nf + 0.29)' nrd='0.29 / W' nrs='0.29 / W'
+ sa=0 sb=0 sd=0 mult=32 m=32
XMPM5[4] net6 VB VDD VDD sky130_fd_pr__pfet_01v8 L=0.15 W=1 nf=1 ad='int((nf+1)/2) * W/nf * 0.29' as='int((nf+2)/2) * W/nf * 0.29'
+ pd='2*int((nf+1)/2) * (W/nf + 0.29)' ps='2*int((nf+2)/2) * (W/nf + 0.29)' nrd='0.29 / W' nrs='0.29 / W'
+ sa=0 sb=0 sd=0 mult=32 m=32
XMPM5[3] net6 VB VDD VDD sky130_fd_pr__pfet_01v8 L=0.15 W=1 nf=1 ad='int((nf+1)/2) * W/nf * 0.29' as='int((nf+2)/2) * W/nf * 0.29'
+ pd='2*int((nf+1)/2) * (W/nf + 0.29)' ps='2*int((nf+2)/2) * (W/nf + 0.29)' nrd='0.29 / W' nrs='0.29 / W'
+ sa=0 sb=0 sd=0 mult=32 m=32
XMPM5[2] net6 VB VDD VDD sky130_fd_pr__pfet_01v8 L=0.15 W=1 nf=1 ad='int((nf+1)/2) * W/nf * 0.29' as='int((nf+2)/2) * W/nf * 0.29'
+ pd='2*int((nf+1)/2) * (W/nf + 0.29)' ps='2*int((nf+2)/2) * (W/nf + 0.29)' nrd='0.29 / W' nrs='0.29 / W'
+ sa=0 sb=0 sd=0 mult=32 m=32
XMPM5[1] net6 VB VDD VDD sky130_fd_pr__pfet_01v8 L=0.15 W=1 nf=1 ad='int((nf+1)/2) * W/nf * 0.29' as='int((nf+2)/2) * W/nf * 0.29'
+ pd='2*int((nf+1)/2) * (W/nf + 0.29)' ps='2*int((nf+2)/2) * (W/nf + 0.29)' nrd='0.29 / W' nrs='0.29 / W'
+ sa=0 sb=0 sd=0 mult=32 m=32
XMPM5[0] net6 VB VDD VDD sky130_fd_pr__pfet_01v8 L=0.15 W=1 nf=1 ad='int((nf+1)/2) * W/nf * 0.29' as='int((nf+2)/2) * W/nf * 0.29'
+ pd='2*int((nf+1)/2) * (W/nf + 0.29)' ps='2*int((nf+2)/2) * (W/nf + 0.29)' nrd='0.29 / W' nrs='0.29 / W'
+ sa=0 sb=0 sd=0 mult=32 m=32
XMPM4[15] net5 VB VDD VDD sky130_fd_pr__pfet_01v8 L=0.15 W=1 nf=1 ad='int((nf+1)/2) * W/nf * 0.29' as='int((nf+2)/2) * W/nf * 0.29'
+ pd='2*int((nf+1)/2) * (W/nf + 0.29)' ps='2*int((nf+2)/2) * (W/nf + 0.29)' nrd='0.29 / W' nrs='0.29 / W'
+ sa=0 sb=0 sd=0 mult=16 m=16
XMPM4[14] net5 VB VDD VDD sky130_fd_pr__pfet_01v8 L=0.15 W=1 nf=1 ad='int((nf+1)/2) * W/nf * 0.29' as='int((nf+2)/2) * W/nf * 0.29'
+ pd='2*int((nf+1)/2) * (W/nf + 0.29)' ps='2*int((nf+2)/2) * (W/nf + 0.29)' nrd='0.29 / W' nrs='0.29 / W'
+ sa=0 sb=0 sd=0 mult=16 m=16
XMPM4[13] net5 VB VDD VDD sky130_fd_pr__pfet_01v8 L=0.15 W=1 nf=1 ad='int((nf+1)/2) * W/nf * 0.29' as='int((nf+2)/2) * W/nf * 0.29'
+ pd='2*int((nf+1)/2) * (W/nf + 0.29)' ps='2*int((nf+2)/2) * (W/nf + 0.29)' nrd='0.29 / W' nrs='0.29 / W'
+ sa=0 sb=0 sd=0 mult=16 m=16
XMPM4[12] net5 VB VDD VDD sky130_fd_pr__pfet_01v8 L=0.15 W=1 nf=1 ad='int((nf+1)/2) * W/nf * 0.29' as='int((nf+2)/2) * W/nf * 0.29'
+ pd='2*int((nf+1)/2) * (W/nf + 0.29)' ps='2*int((nf+2)/2) * (W/nf + 0.29)' nrd='0.29 / W' nrs='0.29 / W'
+ sa=0 sb=0 sd=0 mult=16 m=16
XMPM4[11] net5 VB VDD VDD sky130_fd_pr__pfet_01v8 L=0.15 W=1 nf=1 ad='int((nf+1)/2) * W/nf * 0.29' as='int((nf+2)/2) * W/nf * 0.29'
+ pd='2*int((nf+1)/2) * (W/nf + 0.29)' ps='2*int((nf+2)/2) * (W/nf + 0.29)' nrd='0.29 / W' nrs='0.29 / W'
+ sa=0 sb=0 sd=0 mult=16 m=16
XMPM4[10] net5 VB VDD VDD sky130_fd_pr__pfet_01v8 L=0.15 W=1 nf=1 ad='int((nf+1)/2) * W/nf * 0.29' as='int((nf+2)/2) * W/nf * 0.29'
+ pd='2*int((nf+1)/2) * (W/nf + 0.29)' ps='2*int((nf+2)/2) * (W/nf + 0.29)' nrd='0.29 / W' nrs='0.29 / W'
+ sa=0 sb=0 sd=0 mult=16 m=16
XMPM4[9] net5 VB VDD VDD sky130_fd_pr__pfet_01v8 L=0.15 W=1 nf=1 ad='int((nf+1)/2) * W/nf * 0.29' as='int((nf+2)/2) * W/nf * 0.29'
+ pd='2*int((nf+1)/2) * (W/nf + 0.29)' ps='2*int((nf+2)/2) * (W/nf + 0.29)' nrd='0.29 / W' nrs='0.29 / W'
+ sa=0 sb=0 sd=0 mult=16 m=16
XMPM4[8] net5 VB VDD VDD sky130_fd_pr__pfet_01v8 L=0.15 W=1 nf=1 ad='int((nf+1)/2) * W/nf * 0.29' as='int((nf+2)/2) * W/nf * 0.29'
+ pd='2*int((nf+1)/2) * (W/nf + 0.29)' ps='2*int((nf+2)/2) * (W/nf + 0.29)' nrd='0.29 / W' nrs='0.29 / W'
+ sa=0 sb=0 sd=0 mult=16 m=16
XMPM4[7] net5 VB VDD VDD sky130_fd_pr__pfet_01v8 L=0.15 W=1 nf=1 ad='int((nf+1)/2) * W/nf * 0.29' as='int((nf+2)/2) * W/nf * 0.29'
+ pd='2*int((nf+1)/2) * (W/nf + 0.29)' ps='2*int((nf+2)/2) * (W/nf + 0.29)' nrd='0.29 / W' nrs='0.29 / W'
+ sa=0 sb=0 sd=0 mult=16 m=16
XMPM4[6] net5 VB VDD VDD sky130_fd_pr__pfet_01v8 L=0.15 W=1 nf=1 ad='int((nf+1)/2) * W/nf * 0.29' as='int((nf+2)/2) * W/nf * 0.29'
+ pd='2*int((nf+1)/2) * (W/nf + 0.29)' ps='2*int((nf+2)/2) * (W/nf + 0.29)' nrd='0.29 / W' nrs='0.29 / W'
+ sa=0 sb=0 sd=0 mult=16 m=16
XMPM4[5] net5 VB VDD VDD sky130_fd_pr__pfet_01v8 L=0.15 W=1 nf=1 ad='int((nf+1)/2) * W/nf * 0.29' as='int((nf+2)/2) * W/nf * 0.29'
+ pd='2*int((nf+1)/2) * (W/nf + 0.29)' ps='2*int((nf+2)/2) * (W/nf + 0.29)' nrd='0.29 / W' nrs='0.29 / W'
+ sa=0 sb=0 sd=0 mult=16 m=16
XMPM4[4] net5 VB VDD VDD sky130_fd_pr__pfet_01v8 L=0.15 W=1 nf=1 ad='int((nf+1)/2) * W/nf * 0.29' as='int((nf+2)/2) * W/nf * 0.29'
+ pd='2*int((nf+1)/2) * (W/nf + 0.29)' ps='2*int((nf+2)/2) * (W/nf + 0.29)' nrd='0.29 / W' nrs='0.29 / W'
+ sa=0 sb=0 sd=0 mult=16 m=16
XMPM4[3] net5 VB VDD VDD sky130_fd_pr__pfet_01v8 L=0.15 W=1 nf=1 ad='int((nf+1)/2) * W/nf * 0.29' as='int((nf+2)/2) * W/nf * 0.29'
+ pd='2*int((nf+1)/2) * (W/nf + 0.29)' ps='2*int((nf+2)/2) * (W/nf + 0.29)' nrd='0.29 / W' nrs='0.29 / W'
+ sa=0 sb=0 sd=0 mult=16 m=16
XMPM4[2] net5 VB VDD VDD sky130_fd_pr__pfet_01v8 L=0.15 W=1 nf=1 ad='int((nf+1)/2) * W/nf * 0.29' as='int((nf+2)/2) * W/nf * 0.29'
+ pd='2*int((nf+1)/2) * (W/nf + 0.29)' ps='2*int((nf+2)/2) * (W/nf + 0.29)' nrd='0.29 / W' nrs='0.29 / W'
+ sa=0 sb=0 sd=0 mult=16 m=16
XMPM4[1] net5 VB VDD VDD sky130_fd_pr__pfet_01v8 L=0.15 W=1 nf=1 ad='int((nf+1)/2) * W/nf * 0.29' as='int((nf+2)/2) * W/nf * 0.29'
+ pd='2*int((nf+1)/2) * (W/nf + 0.29)' ps='2*int((nf+2)/2) * (W/nf + 0.29)' nrd='0.29 / W' nrs='0.29 / W'
+ sa=0 sb=0 sd=0 mult=16 m=16
XMPM4[0] net5 VB VDD VDD sky130_fd_pr__pfet_01v8 L=0.15 W=1 nf=1 ad='int((nf+1)/2) * W/nf * 0.29' as='int((nf+2)/2) * W/nf * 0.29'
+ pd='2*int((nf+1)/2) * (W/nf + 0.29)' ps='2*int((nf+2)/2) * (W/nf + 0.29)' nrd='0.29 / W' nrs='0.29 / W'
+ sa=0 sb=0 sd=0 mult=16 m=16
XMPM3[7] net4 VB VDD VDD sky130_fd_pr__pfet_01v8 L=0.15 W=1 nf=1 ad='int((nf+1)/2) * W/nf * 0.29' as='int((nf+2)/2) * W/nf * 0.29'
+ pd='2*int((nf+1)/2) * (W/nf + 0.29)' ps='2*int((nf+2)/2) * (W/nf + 0.29)' nrd='0.29 / W' nrs='0.29 / W'
+ sa=0 sb=0 sd=0 mult=8 m=8
XMPM3[6] net4 VB VDD VDD sky130_fd_pr__pfet_01v8 L=0.15 W=1 nf=1 ad='int((nf+1)/2) * W/nf * 0.29' as='int((nf+2)/2) * W/nf * 0.29'
+ pd='2*int((nf+1)/2) * (W/nf + 0.29)' ps='2*int((nf+2)/2) * (W/nf + 0.29)' nrd='0.29 / W' nrs='0.29 / W'
+ sa=0 sb=0 sd=0 mult=8 m=8
XMPM3[5] net4 VB VDD VDD sky130_fd_pr__pfet_01v8 L=0.15 W=1 nf=1 ad='int((nf+1)/2) * W/nf * 0.29' as='int((nf+2)/2) * W/nf * 0.29'
+ pd='2*int((nf+1)/2) * (W/nf + 0.29)' ps='2*int((nf+2)/2) * (W/nf + 0.29)' nrd='0.29 / W' nrs='0.29 / W'
+ sa=0 sb=0 sd=0 mult=8 m=8
XMPM3[4] net4 VB VDD VDD sky130_fd_pr__pfet_01v8 L=0.15 W=1 nf=1 ad='int((nf+1)/2) * W/nf * 0.29' as='int((nf+2)/2) * W/nf * 0.29'
+ pd='2*int((nf+1)/2) * (W/nf + 0.29)' ps='2*int((nf+2)/2) * (W/nf + 0.29)' nrd='0.29 / W' nrs='0.29 / W'
+ sa=0 sb=0 sd=0 mult=8 m=8
XMPM3[3] net4 VB VDD VDD sky130_fd_pr__pfet_01v8 L=0.15 W=1 nf=1 ad='int((nf+1)/2) * W/nf * 0.29' as='int((nf+2)/2) * W/nf * 0.29'
+ pd='2*int((nf+1)/2) * (W/nf + 0.29)' ps='2*int((nf+2)/2) * (W/nf + 0.29)' nrd='0.29 / W' nrs='0.29 / W'
+ sa=0 sb=0 sd=0 mult=8 m=8
XMPM3[2] net4 VB VDD VDD sky130_fd_pr__pfet_01v8 L=0.15 W=1 nf=1 ad='int((nf+1)/2) * W/nf * 0.29' as='int((nf+2)/2) * W/nf * 0.29'
+ pd='2*int((nf+1)/2) * (W/nf + 0.29)' ps='2*int((nf+2)/2) * (W/nf + 0.29)' nrd='0.29 / W' nrs='0.29 / W'
+ sa=0 sb=0 sd=0 mult=8 m=8
XMPM3[1] net4 VB VDD VDD sky130_fd_pr__pfet_01v8 L=0.15 W=1 nf=1 ad='int((nf+1)/2) * W/nf * 0.29' as='int((nf+2)/2) * W/nf * 0.29'
+ pd='2*int((nf+1)/2) * (W/nf + 0.29)' ps='2*int((nf+2)/2) * (W/nf + 0.29)' nrd='0.29 / W' nrs='0.29 / W'
+ sa=0 sb=0 sd=0 mult=8 m=8
XMPM3[0] net4 VB VDD VDD sky130_fd_pr__pfet_01v8 L=0.15 W=1 nf=1 ad='int((nf+1)/2) * W/nf * 0.29' as='int((nf+2)/2) * W/nf * 0.29'
+ pd='2*int((nf+1)/2) * (W/nf + 0.29)' ps='2*int((nf+2)/2) * (W/nf + 0.29)' nrd='0.29 / W' nrs='0.29 / W'
+ sa=0 sb=0 sd=0 mult=8 m=8
XMPM2[3] net3 VB VDD VDD sky130_fd_pr__pfet_01v8 L=0.15 W=1 nf=1 ad='int((nf+1)/2) * W/nf * 0.29' as='int((nf+2)/2) * W/nf * 0.29'
+ pd='2*int((nf+1)/2) * (W/nf + 0.29)' ps='2*int((nf+2)/2) * (W/nf + 0.29)' nrd='0.29 / W' nrs='0.29 / W'
+ sa=0 sb=0 sd=0 mult=4 m=4
XMPM2[2] net3 VB VDD VDD sky130_fd_pr__pfet_01v8 L=0.15 W=1 nf=1 ad='int((nf+1)/2) * W/nf * 0.29' as='int((nf+2)/2) * W/nf * 0.29'
+ pd='2*int((nf+1)/2) * (W/nf + 0.29)' ps='2*int((nf+2)/2) * (W/nf + 0.29)' nrd='0.29 / W' nrs='0.29 / W'
+ sa=0 sb=0 sd=0 mult=4 m=4
XMPM2[1] net3 VB VDD VDD sky130_fd_pr__pfet_01v8 L=0.15 W=1 nf=1 ad='int((nf+1)/2) * W/nf * 0.29' as='int((nf+2)/2) * W/nf * 0.29'
+ pd='2*int((nf+1)/2) * (W/nf + 0.29)' ps='2*int((nf+2)/2) * (W/nf + 0.29)' nrd='0.29 / W' nrs='0.29 / W'
+ sa=0 sb=0 sd=0 mult=4 m=4
XMPM2[0] net3 VB VDD VDD sky130_fd_pr__pfet_01v8 L=0.15 W=1 nf=1 ad='int((nf+1)/2) * W/nf * 0.29' as='int((nf+2)/2) * W/nf * 0.29'
+ pd='2*int((nf+1)/2) * (W/nf + 0.29)' ps='2*int((nf+2)/2) * (W/nf + 0.29)' nrd='0.29 / W' nrs='0.29 / W'
+ sa=0 sb=0 sd=0 mult=4 m=4
XMPM1[1] net2 VB VDD VDD sky130_fd_pr__pfet_01v8 L=0.15 W=1 nf=1 ad='int((nf+1)/2) * W/nf * 0.29' as='int((nf+2)/2) * W/nf * 0.29'
+ pd='2*int((nf+1)/2) * (W/nf + 0.29)' ps='2*int((nf+2)/2) * (W/nf + 0.29)' nrd='0.29 / W' nrs='0.29 / W'
+ sa=0 sb=0 sd=0 mult=2 m=2
XMPM1[0] net2 VB VDD VDD sky130_fd_pr__pfet_01v8 L=0.15 W=1 nf=1 ad='int((nf+1)/2) * W/nf * 0.29' as='int((nf+2)/2) * W/nf * 0.29'
+ pd='2*int((nf+1)/2) * (W/nf + 0.29)' ps='2*int((nf+2)/2) * (W/nf + 0.29)' nrd='0.29 / W' nrs='0.29 / W'
+ sa=0 sb=0 sd=0 mult=2 m=2
XMPM0 net1 VB VDD VDD sky130_fd_pr__pfet_01v8 L=0.15 W=1 nf=1 ad='int((nf+1)/2) * W/nf * 0.29' as='int((nf+2)/2) * W/nf * 0.29'
+ pd='2*int((nf+1)/2) * (W/nf + 0.29)' ps='2*int((nf+2)/2) * (W/nf + 0.29)' nrd='0.29 / W' nrs='0.29 / W'
+ sa=0 sb=0 sd=0 mult=1 m=1
XMSW0 net1 b0 Vout GND sky130_fd_pr__nfet_01v8 L=0.15 W=1 nf=1 ad='int((nf+1)/2) * W/nf * 0.29' as='int((nf+2)/2) * W/nf * 0.29'
+ pd='2*int((nf+1)/2) * (W/nf + 0.29)' ps='2*int((nf+2)/2) * (W/nf + 0.29)' nrd='0.29 / W' nrs='0.29 / W'
+ sa=0 sb=0 sd=0 mult=1 m=1
XMSW1 net2 b1 Vout GND sky130_fd_pr__nfet_01v8 L=0.15 W=2 nf=1 ad='int((nf+1)/2) * W/nf * 0.29' as='int((nf+2)/2) * W/nf * 0.29'
+ pd='2*int((nf+1)/2) * (W/nf + 0.29)' ps='2*int((nf+2)/2) * (W/nf + 0.29)' nrd='0.29 / W' nrs='0.29 / W'
+ sa=0 sb=0 sd=0 mult=1 m=1
XMSW2 net3 b2 Vout GND sky130_fd_pr__nfet_01v8 L=0.15 W=4 nf=1 ad='int((nf+1)/2) * W/nf * 0.29' as='int((nf+2)/2) * W/nf * 0.29'
+ pd='2*int((nf+1)/2) * (W/nf + 0.29)' ps='2*int((nf+2)/2) * (W/nf + 0.29)' nrd='0.29 / W' nrs='0.29 / W'
+ sa=0 sb=0 sd=0 mult=1 m=1
XMSW3 net4 b3 Vout GND sky130_fd_pr__nfet_01v8 L=0.15 W=8 nf=1 ad='int((nf+1)/2) * W/nf * 0.29' as='int((nf+2)/2) * W/nf * 0.29'
+ pd='2*int((nf+1)/2) * (W/nf + 0.29)' ps='2*int((nf+2)/2) * (W/nf + 0.29)' nrd='0.29 / W' nrs='0.29 / W'
+ sa=0 sb=0 sd=0 mult=1 m=1
XMSW4 net5 b4 Vout GND sky130_fd_pr__nfet_01v8 L=0.15 W=16 nf=1 ad='int((nf+1)/2) * W/nf * 0.29' as='int((nf+2)/2) * W/nf * 0.29'
+ pd='2*int((nf+1)/2) * (W/nf + 0.29)' ps='2*int((nf+2)/2) * (W/nf + 0.29)' nrd='0.29 / W' nrs='0.29 / W'
+ sa=0 sb=0 sd=0 mult=1 m=1
XMSW5 net6 b5 Vout GND sky130_fd_pr__nfet_01v8 L=0.15 W=32 nf=1 ad='int((nf+1)/2) * W/nf * 0.29' as='int((nf+2)/2) * W/nf * 0.29'
+ pd='2*int((nf+1)/2) * (W/nf + 0.29)' ps='2*int((nf+2)/2) * (W/nf + 0.29)' nrd='0.29 / W' nrs='0.29 / W'
+ sa=0 sb=0 sd=0 mult=1 m=1
XMSW6 net7 b6 Vout GND sky130_fd_pr__nfet_01v8 L=0.15 W=64 nf=1 ad='int((nf+1)/2) * W/nf * 0.29' as='int((nf+2)/2) * W/nf * 0.29'
+ pd='2*int((nf+1)/2) * (W/nf + 0.29)' ps='2*int((nf+2)/2) * (W/nf + 0.29)' nrd='0.29 / W' nrs='0.29 / W'
+ sa=0 sb=0 sd=0 mult=1 m=1
V_b0 b0 GND 1
V_b1 b1 GND 1
V_b2 b2 GND 1
V_b3 b3 GND 1
V_b4 b4 GND 1
V_b5 b5 GND 1
V_b6 b6 GND 1
Vouts Vout GND 0
XRBIAS GND VB GND sky130_fd_pr__res_xhigh_po_0p35 L=10.66 mult=1 m=1
**** begin user architecture code

.lib $::SKYWATER_MODELS/sky130.lib.spice tt


.control
  set wr_singlescale
  let mc_runs = 10
  let run = 1

  dowhile run <= mc_runs
     set appendwrite = FALSE
     set wr_vecnames

     foreach vddval 1.6 1.8 2.0
        alter @VDD[dc] = $vddval

        let code = 0
        dowhile code < 128

           let b6 = floor(code/64)%2
           let b5 = floor(code/32)%2
           let b4 = floor(code/16)%2
           let b3 = floor(code/8)%2
           let b2 = floor(code/4)%2
           let b1 = floor(code/2)%2
           let b0 = code%2

           alter V_b6 dc = {1.8*b6}
           alter V_b5 dc = {1.8*b5}
           alter V_b4 dc = {1.8*b4}
           alter V_b3 dc = {1.8*b3}
           alter V_b2 dc = {1.8*b2}
           alter V_b1 dc = {1.8*b1}
           alter V_b0 dc = {1.8*b0}

           save all
           op

           if code eq 0
              wrdata dacrun{$&run}_vdd{$vddval}.txt code v(b0) v(b1) v(b2) v(b3) v(b4) v(b5) v(b6) I(Vouts)
           else
              set appendwrite
              set wr_vecnames = FALSE
              wrdata dacrun{$&run}_vdd{$vddval}.txt code v(b0) v(b1) v(b2) v(b3) v(b4) v(b5) v(b6) I(Vouts)
           end

           let code = code + 1
        end
     end
     reset
     let run = run + 1
  end
.endc

**** end user architecture code
**.ends
.GLOBAL VDD
.GLOBAL GND
.end
